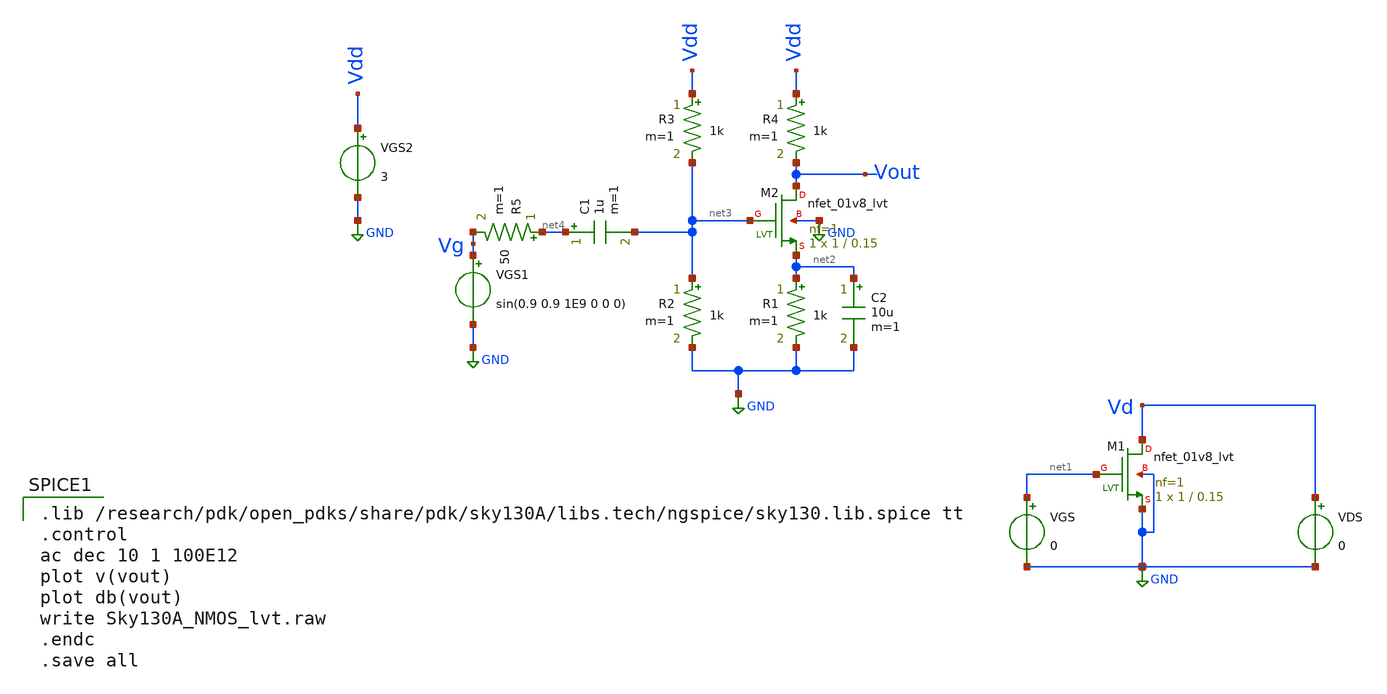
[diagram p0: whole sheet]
** sch_path: skywater_stuff/ECE631_RF_CMOS/untitled.sch
**.subckt untitled
VGS net1 GND 0
VDS Vd GND 0
XM1 Vd net1 GND GND sky130_fd_pr__nfet_01v8_lvt L=0.15 W=1 nf=1 ad='int((nf+1)/2) * W/nf * 0.29' as='int((nf+2)/2) * W/nf * 0.29'
+ pd='2*int((nf+1)/2) * (W/nf + 0.29)' ps='2*int((nf+2)/2) * (W/nf + 0.29)' nrd='0.29 / W' nrs='0.29 / W'
+ sa=0 sb=0 sd=0 mult=1 m=1
XM2 Vout net3 net2 GND sky130_fd_pr__nfet_01v8_lvt L=0.15 W=1 nf=1 ad='int((nf+1)/2) * W/nf * 0.29' as='int((nf+2)/2) * W/nf * 0.29'
+ pd='2*int((nf+1)/2) * (W/nf + 0.29)' ps='2*int((nf+2)/2) * (W/nf + 0.29)' nrd='0.29 / W' nrs='0.29 / W'
+ sa=0 sb=0 sd=0 mult=1 m=1
R1 net2 GND 1k m=1
R2 net3 GND 1k m=1
R3 Vdd net3 1k m=1
R4 Vdd Vout 1k m=1
VGS1 Vg GND sin(0.9 0.9 1E9 0 0 0)
R5 net4 Vg 50 m=1
C1 net4 net3 1u m=1
C2 net2 GND 10u m=1
VGS2 Vdd GND 3
**** begin user architecture code

.lib /research/pdk/open_pdks/share/pdk/sky130A/libs.tech/ngspice/sky130.lib.spice tt
.control
ac dec 10 1 100E12
plot v(vout)
plot db(vout)
write Sky130A_NMOS_lvt.raw
.endc
.save all


**** end user architecture code
**.ends
.GLOBAL GND
.end
